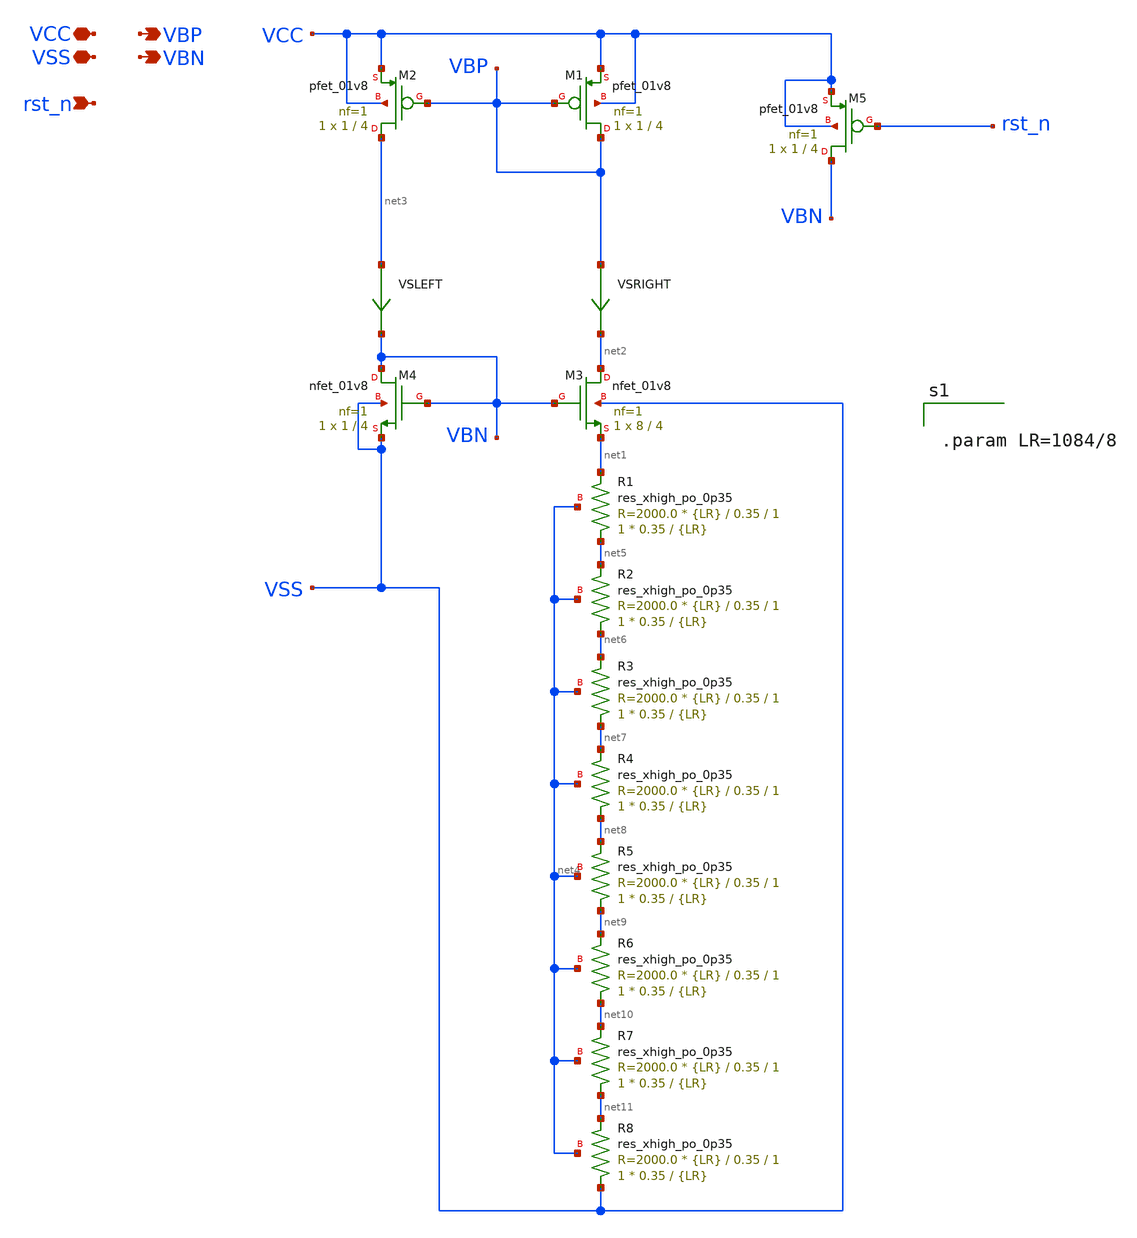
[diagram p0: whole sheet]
** sch_path: schem/bias/bmr_10n.sch
**.subckt bmr_10n VCC VSS rst_n VBP VBN
*.iopin VCC
*.iopin VSS
*.ipin rst_n
*.opin VBP
*.opin VBN
XM1 VBP VBP VCC VCC sky130_fd_pr__pfet_01v8 L=4 W=1 nf=1 ad='int((1 + 1)/2) * 1 / 1 * 0.29' as='int((1 + 2)/2) * 1 / 1 * 0.29'
+ pd='2*int((1 + 1)/2) * (1 / 1 + 0.29)' ps='2*int((1 + 2)/2) * (1 / 1 + 0.29)' nrd='0.29 / 1 ' nrs='0.29 / 1 '
+ sa=0 sb=0 sd=0 mult=1 m=1
XM2 net3 VBP VCC VCC sky130_fd_pr__pfet_01v8 L=4 W=1 nf=1 ad='int((1 + 1)/2) * 1 / 1 * 0.29' as='int((1 + 2)/2) * 1 / 1 * 0.29'
+ pd='2*int((1 + 1)/2) * (1 / 1 + 0.29)' ps='2*int((1 + 2)/2) * (1 / 1 + 0.29)' nrd='0.29 / 1 ' nrs='0.29 / 1 '
+ sa=0 sb=0 sd=0 mult=1 m=1
XM3 net2 VBN net1 VSS sky130_fd_pr__nfet_01v8 L=4 W=8 nf=1 ad='int((1 + 1)/2) * 8 / 1 * 0.29' as='int((1 + 2)/2) * 8 / 1 * 0.29'
+ pd='2*int((1 + 1)/2) * (8 / 1 + 0.29)' ps='2*int((1 + 2)/2) * (8 / 1 + 0.29)' nrd='0.29 / 8 ' nrs='0.29 / 8 '
+ sa=0 sb=0 sd=0 mult=1 m=1
XM4 VBN VBN VSS VSS sky130_fd_pr__nfet_01v8 L=4 W=1 nf=1 ad='int((1 + 1)/2) * 1 / 1 * 0.29' as='int((1 + 2)/2) * 1 / 1 * 0.29'
+ pd='2*int((1 + 1)/2) * (1 / 1 + 0.29)' ps='2*int((1 + 2)/2) * (1 / 1 + 0.29)' nrd='0.29 / 1 ' nrs='0.29 / 1 '
+ sa=0 sb=0 sd=0 mult=1 m=1
XR1 net5 net1 net4 sky130_fd_pr__res_xhigh_po_0p35 L={LR} mult=1 m=1
VSRIGHT VBP net2 0
.save i(vsright)
VSLEFT net3 VBN 0
.save i(vsleft)
XM5 VBN rst_n VCC VCC sky130_fd_pr__pfet_01v8 L=4 W=1 nf=1 ad='int((1 + 1)/2) * 1 / 1 * 0.29' as='int((1 + 2)/2) * 1 / 1 * 0.29'
+ pd='2*int((1 + 1)/2) * (1 / 1 + 0.29)' ps='2*int((1 + 2)/2) * (1 / 1 + 0.29)' nrd='0.29 / 1 ' nrs='0.29 / 1 '
+ sa=0 sb=0 sd=0 mult=1 m=1
XR2 net6 net5 net4 sky130_fd_pr__res_xhigh_po_0p35 L={LR} mult=1 m=1
XR3 net7 net6 net4 sky130_fd_pr__res_xhigh_po_0p35 L={LR} mult=1 m=1
XR4 net8 net7 net4 sky130_fd_pr__res_xhigh_po_0p35 L={LR} mult=1 m=1
XR5 net9 net8 net4 sky130_fd_pr__res_xhigh_po_0p35 L={LR} mult=1 m=1
XR6 net10 net9 net4 sky130_fd_pr__res_xhigh_po_0p35 L={LR} mult=1 m=1
XR7 net11 net10 net4 sky130_fd_pr__res_xhigh_po_0p35 L={LR} mult=1 m=1
XR8 VSS net11 net4 sky130_fd_pr__res_xhigh_po_0p35 L={LR} mult=1 m=1
**** begin user architecture code


.param LR=1084/8


**** end user architecture code
**.ends
.end
